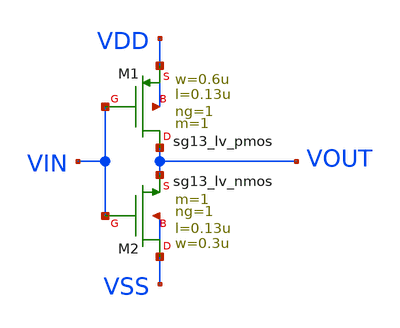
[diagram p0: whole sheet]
** sch_path: Taller3/Insumos/inv_lv.sch
**.subckt inv_lv
XM2 VSS VIN VOUT VSS sg13_lv_nmos w=0.3u l=0.13u ng=1 m=1 mm_ok=1
XM1 VOUT VIN VDD VDD sg13_lv_pmos w=0.6u l=0.13u ng=1 m=1 mm_ok=1
**.ends
.end
